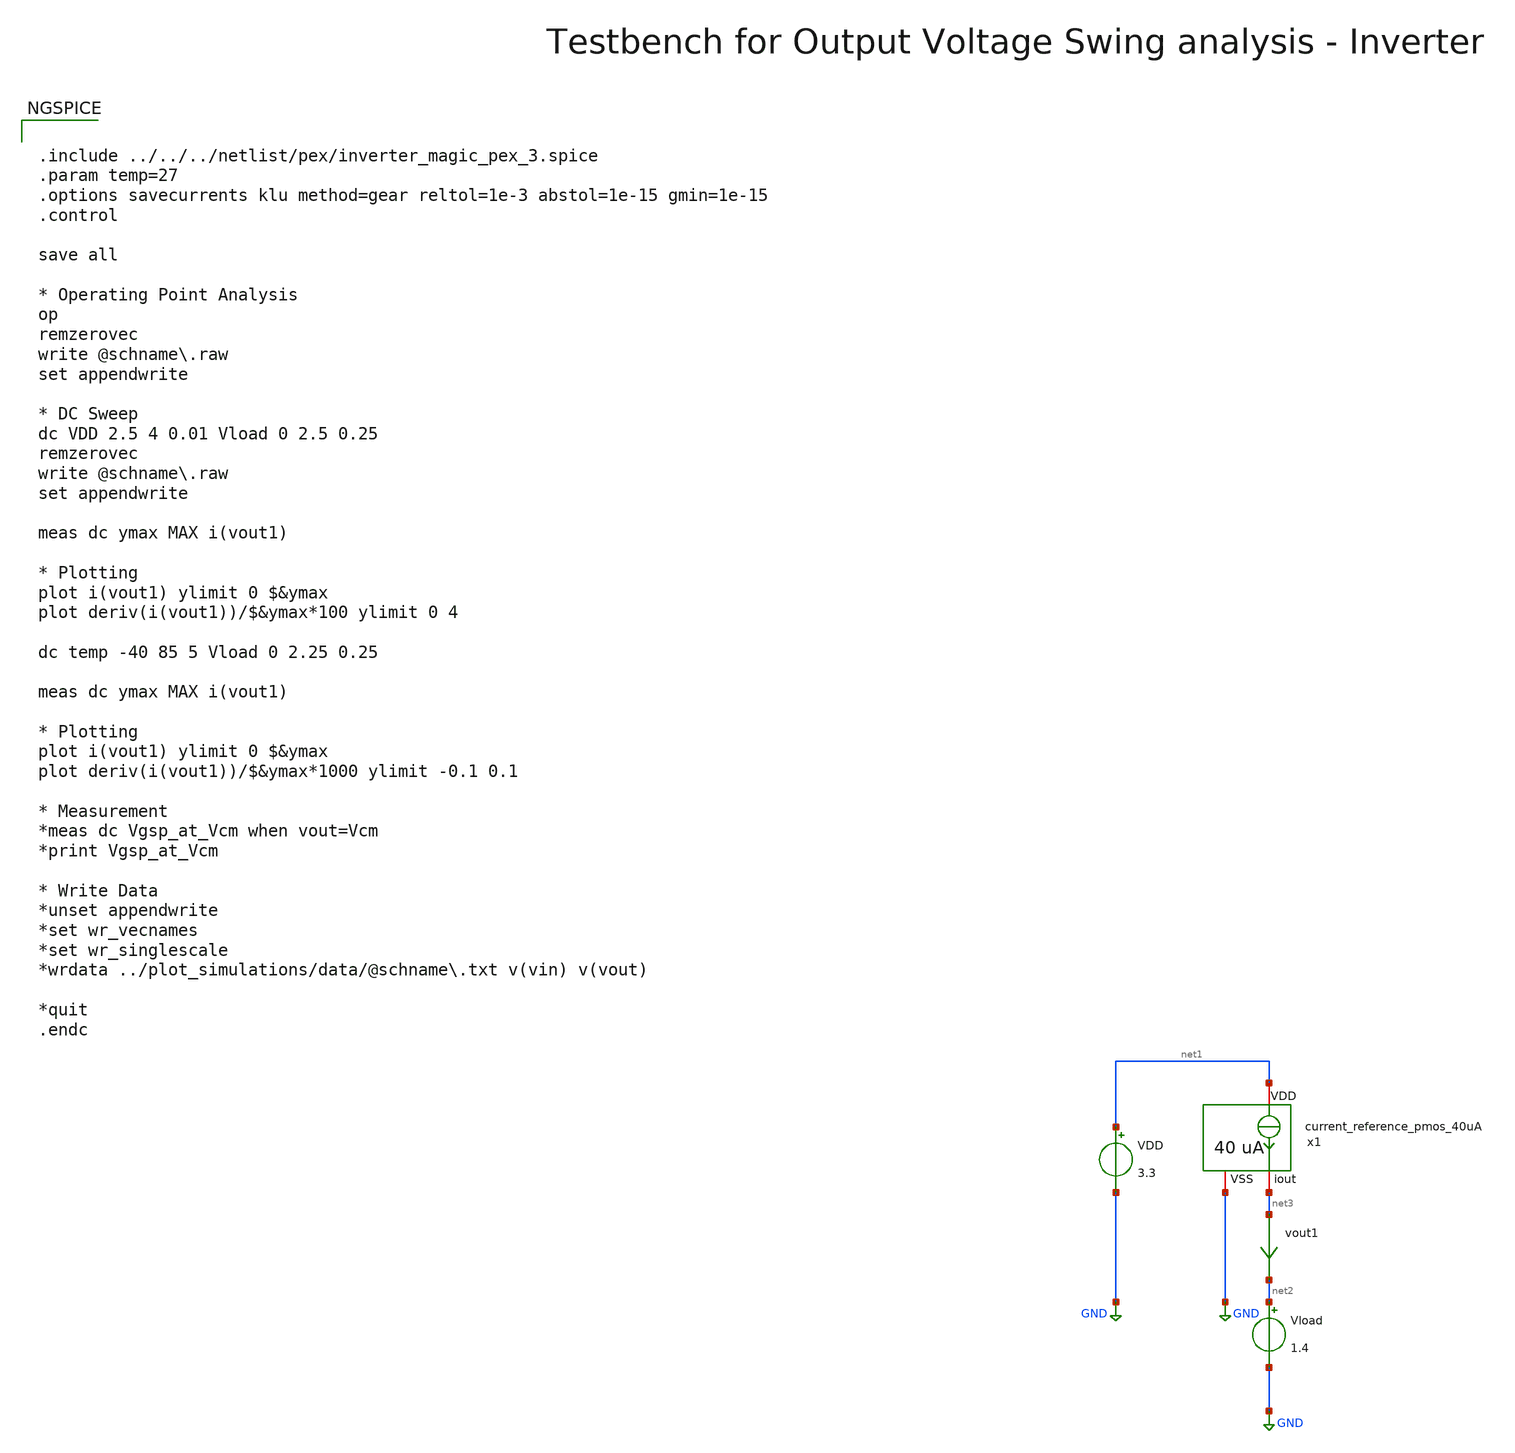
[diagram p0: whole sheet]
** sch_path: macros/heichips26_vcr/macros/switched_capacitor/testbenches/xschem/tb_current_reference_pmos_dc.sch
**.subckt tb_current_reference_pmos_dc
VDD net1 GND 3.3
vout1 net3 net2 0
.save i(vout1)
x1 net1 net3 GND current_reference_pmos_40uA
Vload net2 GND 1.4
**** begin user architecture code


.include ../../../netlist/pex/inverter_magic_pex_3.spice
.param temp=27
.options savecurrents klu method=gear reltol=1e-3 abstol=1e-15 gmin=1e-15
.control

save all

* Operating Point Analysis
op
remzerovec
write @schname\.raw
set appendwrite

* DC Sweep
dc VDD 2.5 4 0.01 Vload 0 2.5 0.25
remzerovec
write @schname\.raw
set appendwrite

meas dc ymax MAX i(vout1)

* Plotting
plot i(vout1) ylimit 0 $&ymax
plot deriv(i(vout1))/$&ymax*100 ylimit 0 4

dc temp -40 85 5 Vload 0 2.25 0.25

meas dc ymax MAX i(vout1)

* Plotting
plot i(vout1) ylimit 0 $&ymax
plot deriv(i(vout1))/$&ymax*1000 ylimit -0.1 0.1

* Measurement
*meas dc Vgsp_at_Vcm when vout=Vcm
*print Vgsp_at_Vcm

* Write Data
*unset appendwrite
*set wr_vecnames
*set wr_singlescale
*wrdata ../plot_simulations/data/@schname\.txt v(vin) v(vout)

*quit
.endc



.lib cornerMOSlv.lib mos_tt
.lib cornerMOShv.lib mos_tt
.lib cornerRES.lib res_typ
.lib cornerDIO.lib dio_tt

**** end user architecture code
**.ends

* expanding   symbol:  current_reference_pmos_40uA.sym # of pins=3
** sym_path: macros/heichips26_vcr/macros/switched_capacitor/schematic/xschem/current_reference_pmos_40uA.sym
** sch_path: macros/heichips26_vcr/macros/switched_capacitor/schematic/xschem/current_reference_pmos_40uA.sch
.subckt current_reference_pmos_40uA VDD iout VSS
*.iopin VSS
*.iopin VDD
*.iopin iout
XM8 net1 net2 VSS VSS sg13_hv_nmos w=n_w l=n_l ng=1 m=1 mm_ok=1
XM6 net1 net1 VDD VDD sg13_hv_pmos w=p_w l=p_l ng=1 m=1 mm_ok=1
XM1 net2 net1 net3 VDD sg13_hv_pmos w=p_w l=p_l ng=1 m=1 mm_ok=1
XM3 net2 net2 VSS VSS sg13_hv_nmos w=n_w l=n_l ng=1 m=1 mm_ok=1
XR2 VDD net4 VSS rppd w=2e-6 l=21.6e-6 m=1 b=0 mm_ok=1
XR3 net4 net3 VSS rsil w=0.5e-6 l=282e-6 m=1 mm_ok=1
**** begin user architecture code


.param n_w = 6u
.param n_l = 5u
.param p_w = 10u
.param p_l = 2u


**** end user architecture code
XM2 net2 net1 net3 VDD sg13_hv_pmos w=p_w l=p_l ng=1 m=1 mm_ok=1
XM4 net2 net1 net3 VDD sg13_hv_pmos w=p_w l=p_l ng=1 m=1 mm_ok=1
XM5 net2 net1 net3 VDD sg13_hv_pmos w=p_w l=p_l ng=1 m=1 mm_ok=1
XM7 iout net1 VDD VDD sg13_hv_pmos w=p_w l=p_l ng=1 m=1 mm_ok=1
.ends

.GLOBAL GND
.end
